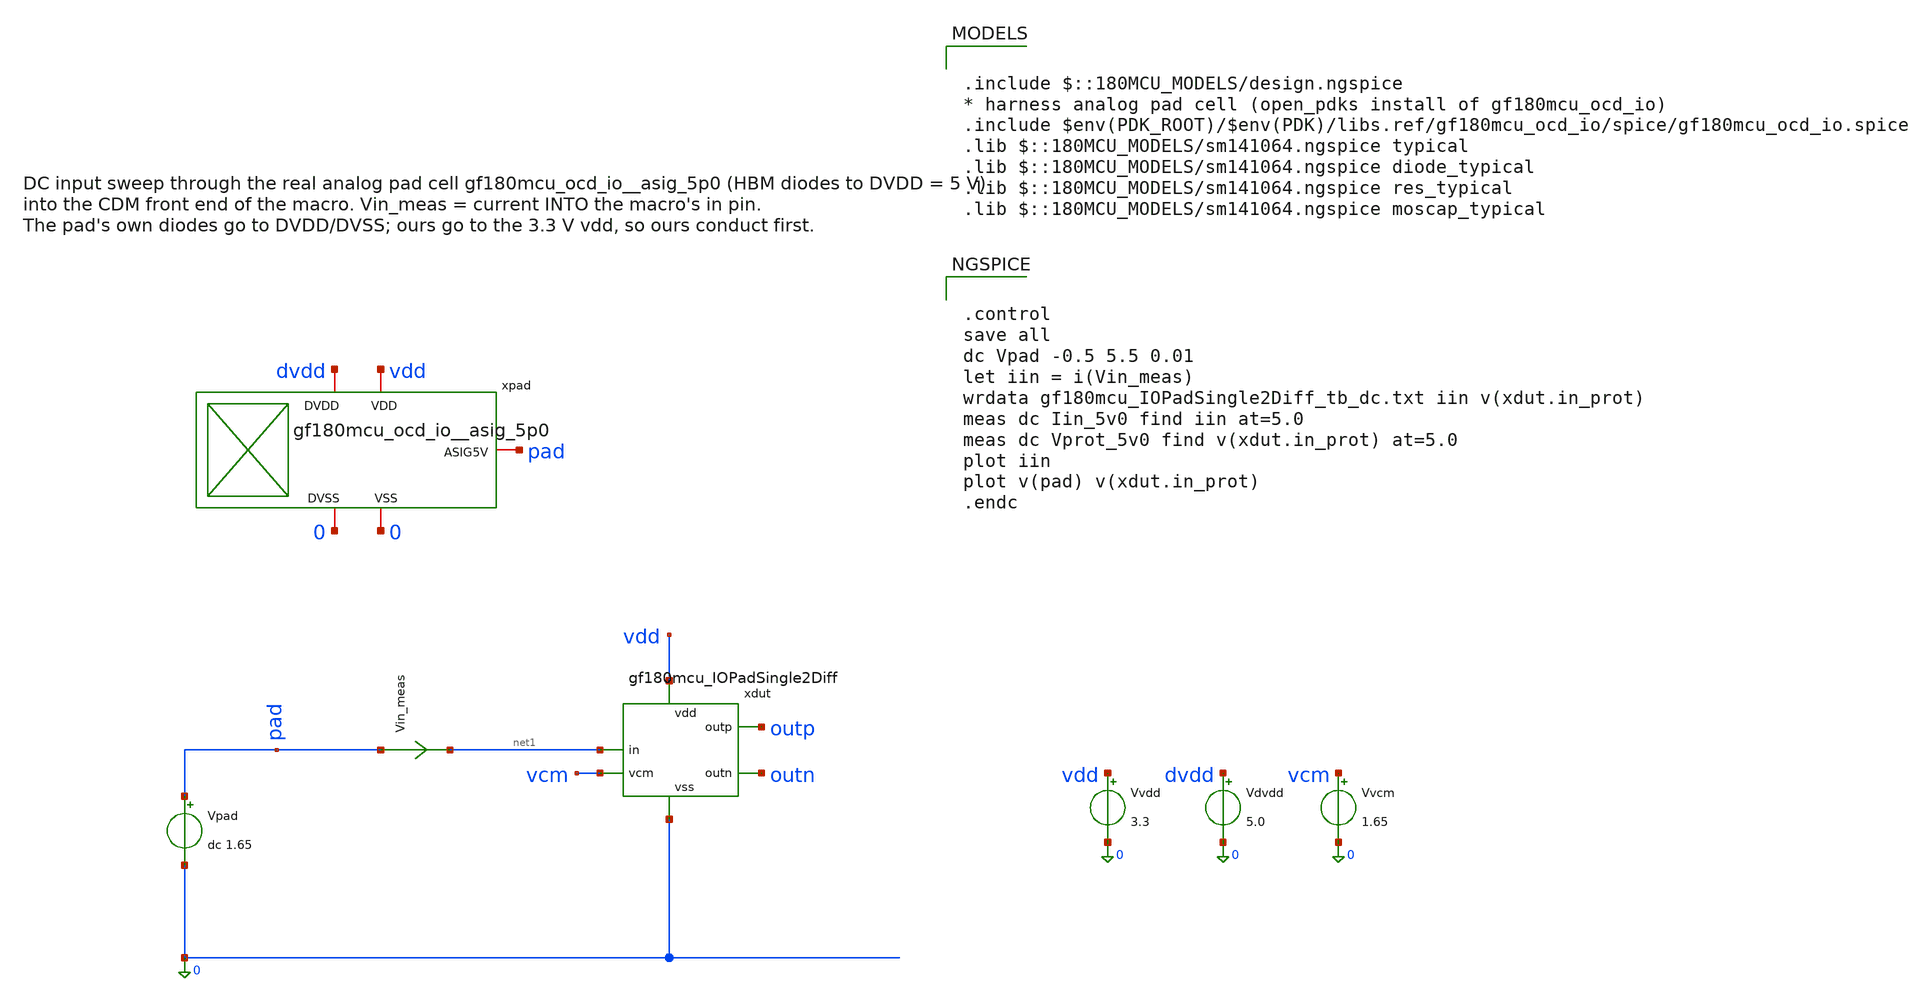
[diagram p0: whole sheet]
** sch_path: macros/gf180mcu_IOPadSingle2Diff/testbenches/xschem/gf180mcu_IOPadSingle2Diff_tb_dc.sch
**.subckt gf180mcu_IOPadSingle2Diff_tb_dc
Vvdd vdd 0 3.3
Vdvdd dvdd 0 5.0
Vvcm vcm 0 1.65
Vpad pad 0 dc 1.65
Vin_meas pad net1 0
.save i(vin_meas)
xdut vdd outp vcm net1 outn 0 gf180mcu_IOPadSingle2Diff
xpad pad dvdd 0 vdd 0 gf180mcu_ocd_io__asig_5p0
**** begin user architecture code


.control
save all
dc Vpad -0.5 5.5 0.01
let iin = i(Vin_meas)
wrdata gf180mcu_IOPadSingle2Diff_tb_dc.txt iin v(xdut.in_prot)
meas dc Iin_5v0 find iin at=5.0
meas dc Vprot_5v0 find v(xdut.in_prot) at=5.0
plot iin
plot v(pad) v(xdut.in_prot)
.endc



.include $::180MCU_MODELS/design.ngspice
* harness analog pad cell (open_pdks install of gf180mcu_ocd_io)
.include $env(PDK_ROOT)/$env(PDK)/libs.ref/gf180mcu_ocd_io/spice/gf180mcu_ocd_io.spice
.lib $::180MCU_MODELS/sm141064.ngspice typical
.lib $::180MCU_MODELS/sm141064.ngspice diode_typical
.lib $::180MCU_MODELS/sm141064.ngspice res_typical
.lib $::180MCU_MODELS/sm141064.ngspice moscap_typical

**** end user architecture code
**.ends

* expanding   symbol:  gf180mcu_IOPadSingle2Diff.sym # of pins=6
** sym_path: macros/gf180mcu_IOPadSingle2Diff/schematic/xschem/gf180mcu_IOPadSingle2Diff.sym
** sch_path: macros/gf180mcu_IOPadSingle2Diff/schematic/xschem/gf180mcu_IOPadSingle2Diff.sch
.subckt gf180mcu_IOPadSingle2Diff vdd outp vcm in outn vss
*.iopin vdd
*.opin outp
*.ipin vcm
*.ipin in
*.opin outn
*.iopin vss
XRcdm in_prot in vss ppolyf_u_1k_6p0 r_width=5e-6 r_length=1e-6 m=1
Dcdmp in_prot vdd diode_pd2nw_06v0 area='2u * 12u ' pj='2*2u + 2*12u ' m=1
Dcdmn vss in_prot diode_nd2ps_06v0 area='2u * 12u ' pj='2*2u + 2*12u ' m=1
.ends

.end
